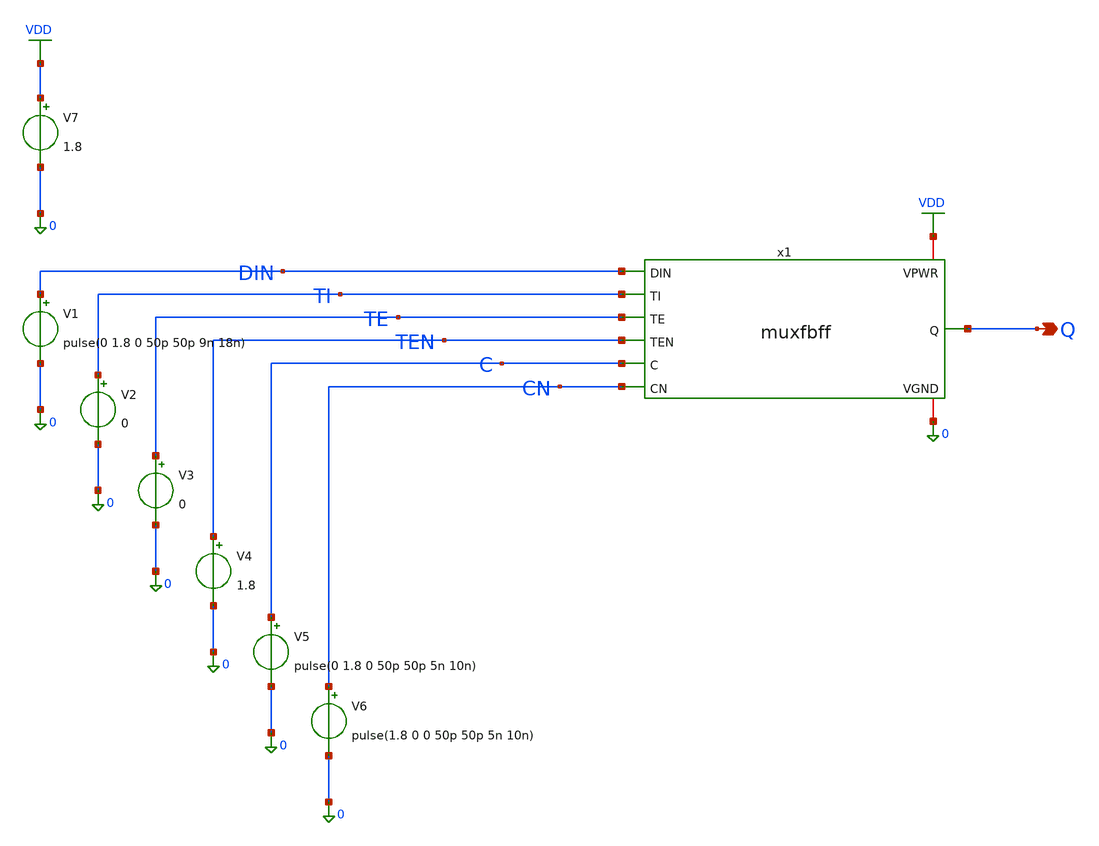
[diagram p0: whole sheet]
** sch_path: muxfbff/muxfbff_tb_setup_calc.sch
**.subckt muxfbff_tb_setup_calc Q
*.opin Q
x1 VDD 0 Q DIN TI TE TEN C CN muxfbff
V1 DIN 0 pulse(0 1.8 0 50p 50p 9n 18n)
V2 TI 0 0
V3 TE 0 0
V4 TEN 0 1.8
V5 C 0 pulse(0 1.8 0 50p 50p 5n 10n)
V6 CN 0 pulse(1.8 0 0 50p 50p 5n 10n)
V7 VDD 0 1.8
**** begin user architecture code

** opencircuitdesign pdks install
.lib $::SKYWATER_MODELS/sky130.lib.spice tt




.tran 0.0001n 30n
.control
  save all
    run
	meas tran delay TRIG v(C) VAL=0.9 RISE=3 TARG v(Q) VAL=0.9 RISE=1
	write /home/sushanth/.xschem/simulations/output.raw
  end
.endc





**** end user architecture code
**.ends
.GLOBAL VDD
.end
